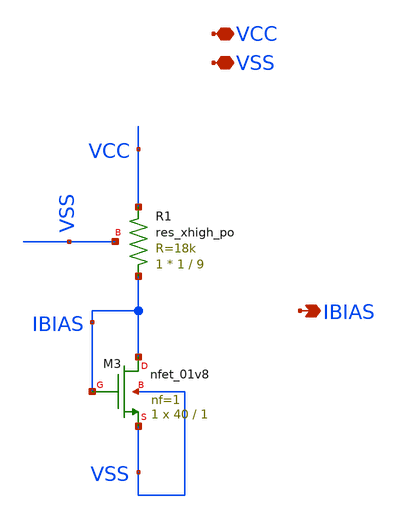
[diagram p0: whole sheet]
** sch_path: xschem/current_source.sch
**.subckt current_source VCC VSS IBIAS
*.iopin VCC
*.iopin VSS
*.opin IBIAS
XM3 IBIAS IBIAS VSS VSS sky130_fd_pr__nfet_01v8 L=1 W=40 nf=1 ad='int((nf+1)/2) * W/nf * 0.29' as='int((nf+2)/2) * W/nf * 0.29'
+ pd='2*int((nf+1)/2) * (W/nf + 0.29)' ps='2*int((nf+2)/2) * (W/nf + 0.29)' nrd='0.29 / W' nrs='0.29 / W'
+ sa=0 sb=0 sd=0 mult=1 m=1
XR1 IBIAS VCC VSS sky130_fd_pr__res_xhigh_po W=1 L=9 mult=1 m=1
**.ends
.end
